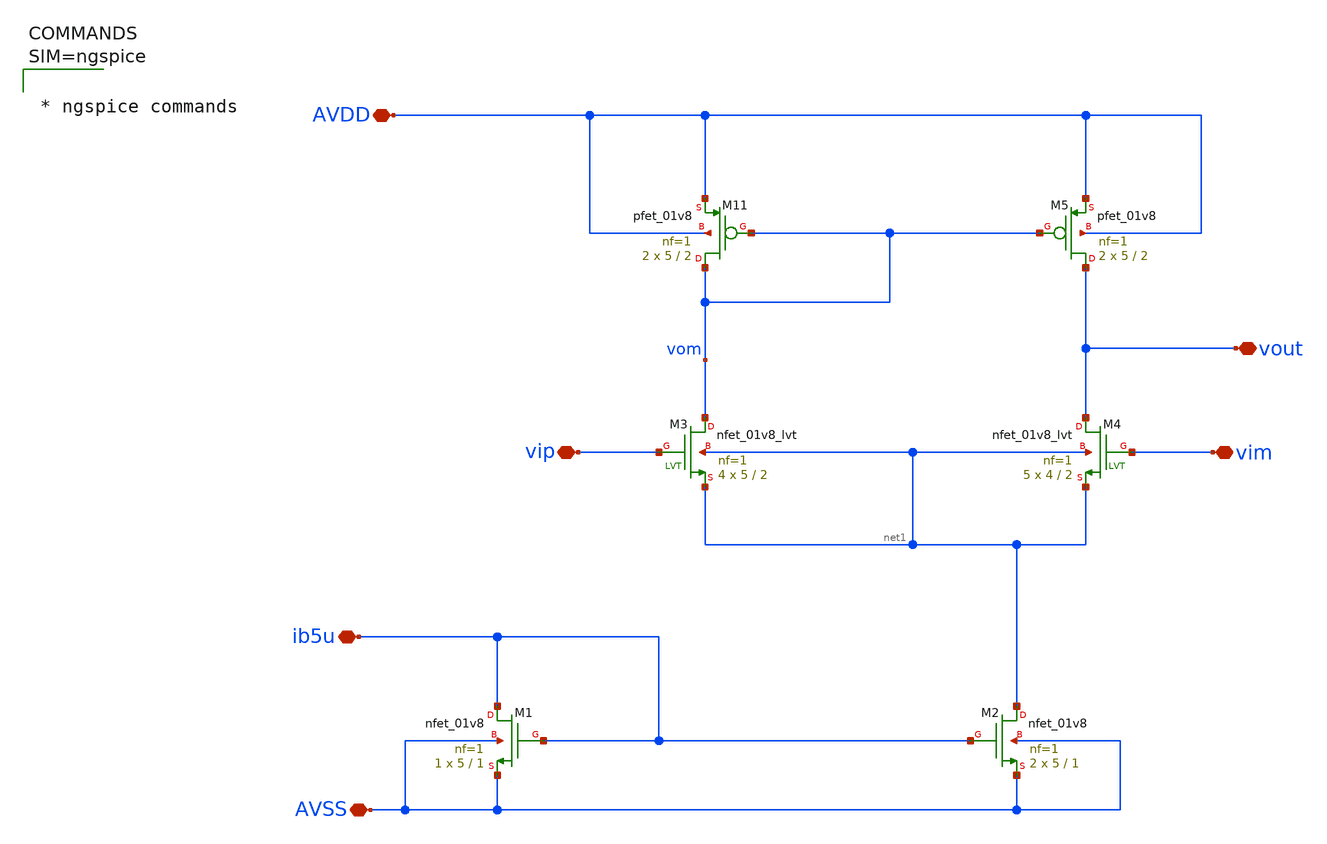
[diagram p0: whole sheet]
** sch_path: xschem/opa_nmos1.sch
**.subckt opa_nmos1 vip vim vout ib5u AVDD AVSS
*.iopin vip
*.iopin vim
*.iopin vout
*.iopin ib5u
*.iopin AVDD
*.iopin AVSS
XM1 ib5u ib5u AVSS AVSS sky130_fd_pr__nfet_01v8 L=1 W=5 nf=1 ad='int((1 + 1)/2) * 5 / 1 * 0.29' as='int((1 + 2)/2) * 5 / 1 * 0.29'
+ pd='2*int((1 + 1)/2) * (5 / 1 + 0.29)' ps='2*int((1 + 2)/2) * (5 / 1 + 0.29)' nrd='0.29 / 5 ' nrs='0.29 / 5 '
+ sa=0 sb=0 sd=0 mult=1 m=1
XM2 net1 ib5u AVSS AVSS sky130_fd_pr__nfet_01v8 L=1 W=5 nf=1 ad='int((1 + 1)/2) * 5 / 1 * 0.29' as='int((1 + 2)/2) * 5 / 1 * 0.29'
+ pd='2*int((1 + 1)/2) * (5 / 1 + 0.29)' ps='2*int((1 + 2)/2) * (5 / 1 + 0.29)' nrd='0.29 / 5 ' nrs='0.29 / 5 '
+ sa=0 sb=0 sd=0 mult=2 m=2
XM3 vom vip net1 net1 sky130_fd_pr__nfet_01v8_lvt L=2 W=5 nf=1 ad='int((1 + 1)/2) * 5 / 1 * 0.29' as='int((1 + 2)/2) * 5 / 1 * 0.29'
+ pd='2*int((1 + 1)/2) * (5 / 1 + 0.29)' ps='2*int((1 + 2)/2) * (5 / 1 + 0.29)' nrd='0.29 / 5 ' nrs='0.29 / 5 '
+ sa=0 sb=0 sd=0 mult=4 m=4
XM4 vout vim net1 net1 sky130_fd_pr__nfet_01v8_lvt L=2 W=4 nf=1 ad='int((1 + 1)/2) * 4 / 1 * 0.29' as='int((1 + 2)/2) * 4 / 1 * 0.29'
+ pd='2*int((1 + 1)/2) * (4 / 1 + 0.29)' ps='2*int((1 + 2)/2) * (4 / 1 + 0.29)' nrd='0.29 / 4 ' nrs='0.29 / 4 '
+ sa=0 sb=0 sd=0 mult=5 m=5
XM11 vom vom AVDD AVDD sky130_fd_pr__pfet_01v8 L=2 W=5 nf=1 ad='int((nf+1)/2) * W/nf * 0.29' as='int((nf+2)/2) * W/nf * 0.29'
+ pd='2*int((nf+1)/2) * (W/nf + 0.29)' ps='2*int((nf+2)/2) * (W/nf + 0.29)' nrd='0.29 / W' nrs='0.29 / W'
+ sa=0 sb=0 sd=0 mult=2 m=2
XM5 vout vom AVDD AVDD sky130_fd_pr__pfet_01v8 L=2 W=5 nf=1 ad='int((nf+1)/2) * W/nf * 0.29' as='int((nf+2)/2) * W/nf * 0.29'
+ pd='2*int((nf+1)/2) * (W/nf + 0.29)' ps='2*int((nf+2)/2) * (W/nf + 0.29)' nrd='0.29 / W' nrs='0.29 / W'
+ sa=0 sb=0 sd=0 mult=2 m=2
**** begin user architecture code

** opencircuitdesign pdks install
.lib $::SKYWATER_MODELS/sky130.lib.spice tt




* ngspice commands




**** end user architecture code
**.ends
.end
